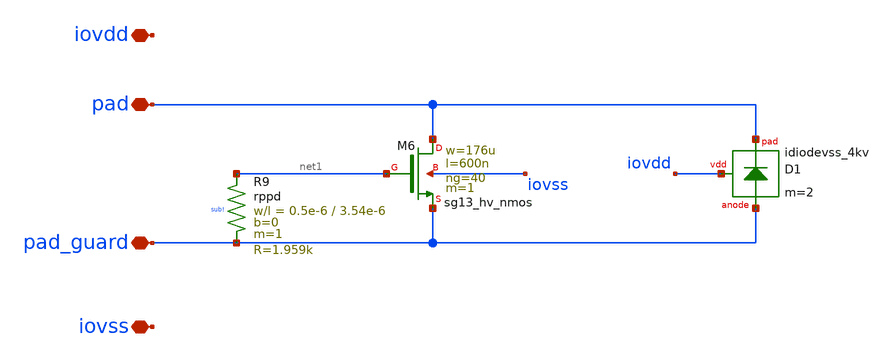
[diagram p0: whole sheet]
** sch_path: trident_test_structures/design_data/xschem/IOPadAnalogGuardLayer/pad_guard_to_vss_first_stage_esd.sch
**.subckt pad_guard_to_vss_first_stage_esd iovss pad_guard iovdd pad
*.iopin iovss
*.iopin pad_guard
*.iopin iovdd
*.iopin pad
XM6 pad net1 pad_guard iovss sg13_hv_nmos w=176u l=600n ng=40 m=1 mm_ok=1
XR9 net1 pad_guard sub! rppd w=0.5e-6 l=3.54e-6 m=1 b=0 mm_ok=1
XD1 iovdd pad pad_guard idiodevss_4kv m=2
**.ends
.end
